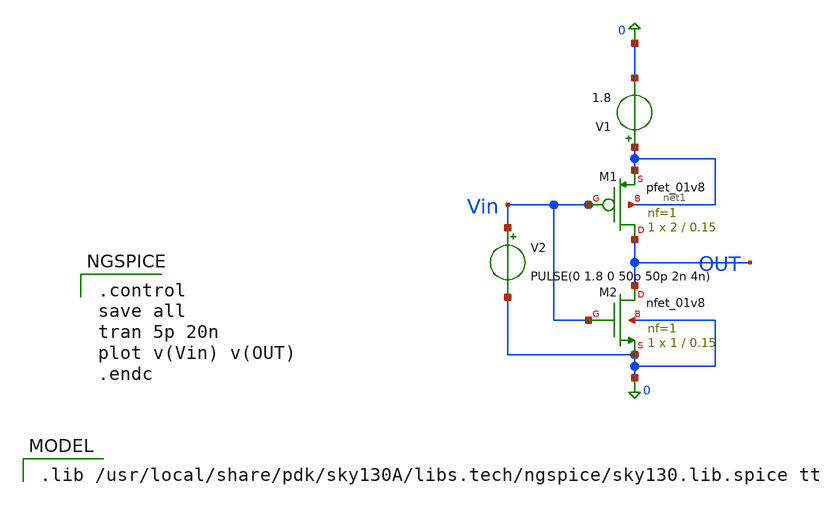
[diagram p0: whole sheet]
** sch_path: inverter_test.sch
**.subckt inverter_test
XM1 OUT Vin net1 net1 sky130_fd_pr__pfet_01v8 L=0.15 W=2 nf=1 ad='int((1 + 1)/2) * 2 / 1 * 0.29' as='int((1 + 2)/2) * 2 / 1 * 0.29'
+ pd='2*int((1 + 1)/2) * (2 / 1 + 0.29)' ps='2*int((1 + 2)/2) * (2 / 1 + 0.29)' nrd='0.29 / 2 ' nrs='0.29 / 2 '
+ sa=0 sb=0 sd=0 mult=1 m=1
XM2 OUT Vin 0 0 sky130_fd_pr__nfet_01v8 L=0.15 W=1 nf=1 ad='int((1 + 1)/2) * 1 / 1 * 0.29' as='int((1 + 2)/2) * 1 / 1 * 0.29'
+ pd='2*int((1 + 1)/2) * (1 / 1 + 0.29)' ps='2*int((1 + 2)/2) * (1 / 1 + 0.29)' nrd='0.29 / 1 ' nrs='0.29 / 1 '
+ sa=0 sb=0 sd=0 mult=1 m=1
V1 net1 0 1.8
V2 Vin 0 PULSE(0 1.8 0 50p 50p 2n 4n)
**** begin user architecture code

.lib /usr/local/share/pdk/sky130A/libs.tech/ngspice/sky130.lib.spice tt


.control
save all
tran 5p 20n
plot v(Vin) v(OUT)
.endc

**** end user architecture code
**.ends
.end
